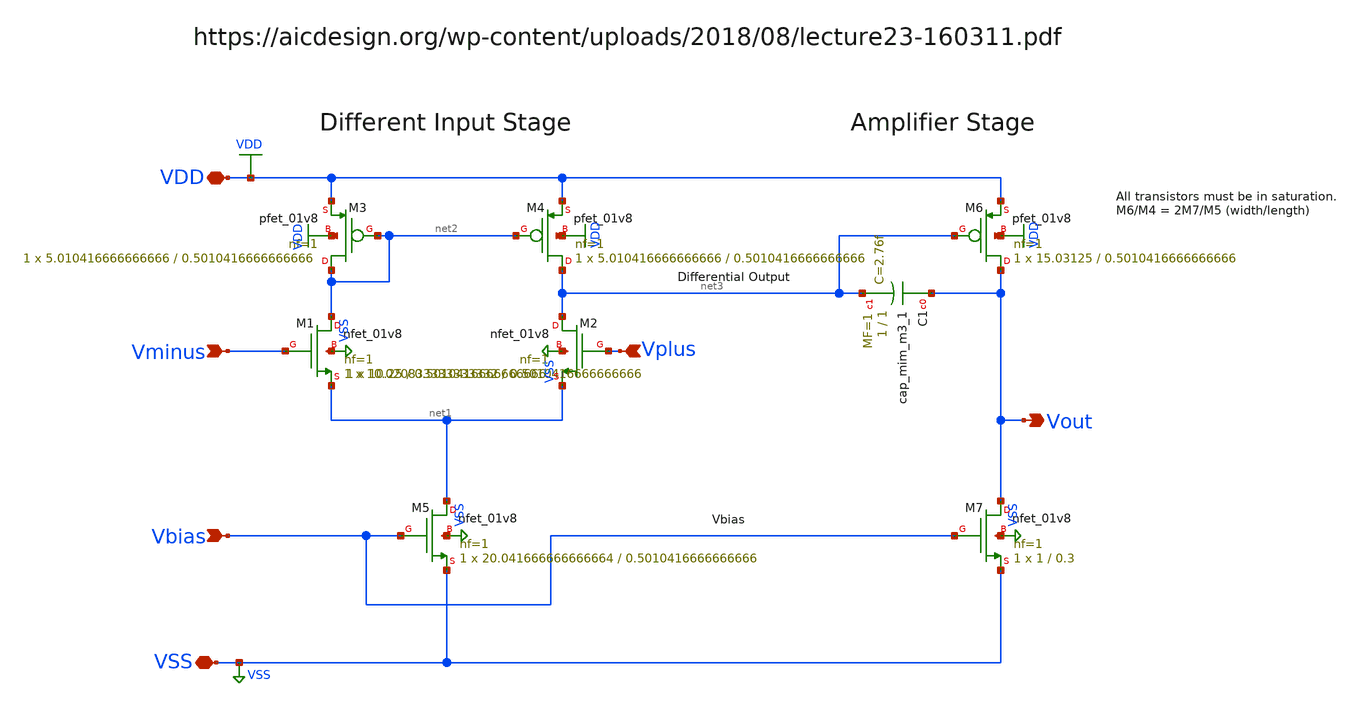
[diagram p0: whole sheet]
** sch_path: examples/template/temp_schemsym_2550c5bd46b84c7187af88445c3944bd.sch
**.subckt temp_schemsym_2550c5bd46b84c7187af88445c3944bd Vplus Vminus VDD VSS Vbias Vout
*.ipin Vplus
*.ipin Vminus
*.iopin VDD
*.iopin VSS
*.ipin Vbias
*.opin Vout
XM1 net2 Vminus net1 VSS sky130_fd_pr__nfet_01v8 L=0.5010416666666666 W=10.020833333333332 nf=1 ad='int((nf+1)/2) * W/nf * 0.29'
+ as='int((nf+2)/2) * W/nf * 0.29' pd='2*int((nf+1)/2) * (W/nf + 0.29)' ps='2*int((nf+2)/2) * (W/nf + 0.29)'
+ nrd='0.29 / W' nrs='0.29 / W' sa=0 sb=0 sd=0 mult=1 m=1
XM2 net3 Vplus net1 VSS sky130_fd_pr__nfet_01v8 L=0.5010416666666666 W=10.25 nf=1 ad='int((nf+1)/2) * W/nf * 0.29'
+ as='int((nf+2)/2) * W/nf * 0.29' pd='2*int((nf+1)/2) * (W/nf + 0.29)' ps='2*int((nf+2)/2) * (W/nf + 0.29)'
+ nrd='0.29 / W' nrs='0.29 / W' sa=0 sb=0 sd=0 mult=1 m=1
XM3 net2 net2 VDD VDD sky130_fd_pr__pfet_01v8 L=0.5010416666666666 W=5.010416666666666 nf=1 ad='int((nf+1)/2) * W/nf * 0.29'
+ as='int((nf+2)/2) * W/nf * 0.29' pd='2*int((nf+1)/2) * (W/nf + 0.29)' ps='2*int((nf+2)/2) * (W/nf + 0.29)'
+ nrd='0.29 / W' nrs='0.29 / W' sa=0 sb=0 sd=0 mult=1 m=1
XM4 net3 net2 VDD VDD sky130_fd_pr__pfet_01v8 L=0.5010416666666666 W=5.010416666666666 nf=1 ad='int((nf+1)/2) * W/nf * 0.29'
+ as='int((nf+2)/2) * W/nf * 0.29' pd='2*int((nf+1)/2) * (W/nf + 0.29)' ps='2*int((nf+2)/2) * (W/nf + 0.29)'
+ nrd='0.29 / W' nrs='0.29 / W' sa=0 sb=0 sd=0 mult=1 m=1
XM5 net1 Vbias VSS VSS sky130_fd_pr__nfet_01v8 L=0.5010416666666666 W=20.041666666666664 nf=1 ad='int((nf+1)/2) * W/nf * 0.29'
+ as='int((nf+2)/2) * W/nf * 0.29' pd='2*int((nf+1)/2) * (W/nf + 0.29)' ps='2*int((nf+2)/2) * (W/nf + 0.29)'
+ nrd='0.29 / W' nrs='0.29 / W' sa=0 sb=0 sd=0 mult=1 m=1
XM6 Vout net3 VDD VDD sky130_fd_pr__pfet_01v8 L=0.5010416666666666 W=15.03125 nf=1 ad='int((nf+1)/2) * W/nf * 0.29'
+ as='int((nf+2)/2) * W/nf * 0.29' pd='2*int((nf+1)/2) * (W/nf + 0.29)' ps='2*int((nf+2)/2) * (W/nf + 0.29)'
+ nrd='0.29 / W' nrs='0.29 / W' sa=0 sb=0 sd=0 mult=1 m=1
XC1 Vout net3 sky130_fd_pr__cap_mim_m3_1 W=1 L=1 MF=1 m=1
XM7 Vout Vbias VSS VSS sky130_fd_pr__nfet_01v8 L=0.3 W=1 nf=1 ad='int((nf+1)/2) * W/nf * 0.29' as='int((nf+2)/2) * W/nf * 0.29'
+ pd='2*int((nf+1)/2) * (W/nf + 0.29)' ps='2*int((nf+2)/2) * (W/nf + 0.29)' nrd='0.29 / W' nrs='0.29 / W'
+ sa=0 sb=0 sd=0 mult=1 m=1
**.ends
.GLOBAL VDD
.GLOBAL VSS
.end
